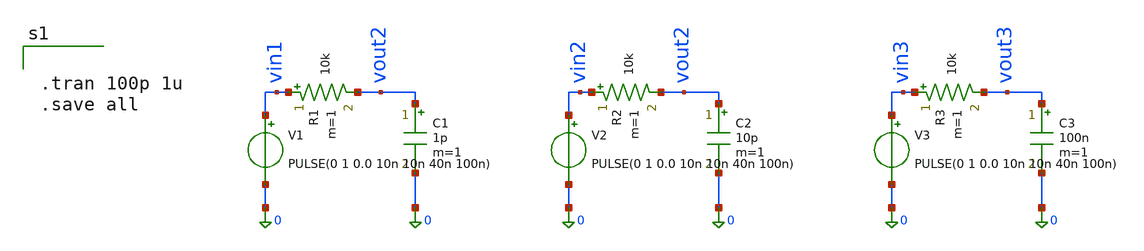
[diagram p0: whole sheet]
** sch_path: experiments/cap_test.sch
**.subckt cap_test
C1 vout2 0 1p m=1
R1 vin1 vout2 10k m=1
V1 vin1 0 PULSE(0 1 0.0 10n 10n 40n 100n)
C2 vout2 0 10p m=1
R2 vin2 vout2 10k m=1
V2 vin2 0 PULSE(0 1 0.0 10n 10n 40n 100n)
C3 vout3 0 100n m=1
R3 vin3 vout3 10k m=1
V3 vin3 0 PULSE(0 1 0.0 10n 10n 40n 100n)
**** begin user architecture code


.tran 100p 1u
.save all


**** end user architecture code
**.ends
.end
